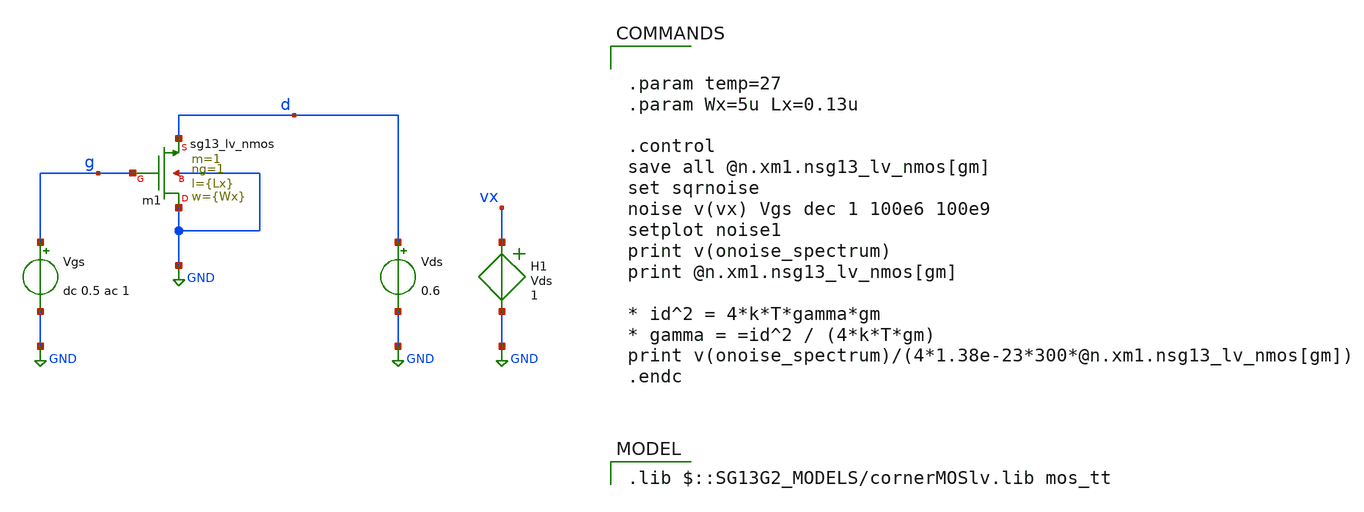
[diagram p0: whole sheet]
** sch_path: 4_Technology/src/tb_sg13_lv_nmos_noise.sch
**.subckt tb_sg13_lv_nmos_noise
Xm1 GND g d GND sg13_lv_nmos w={Wx} l={Lx} ng=1 m=1 mm_ok=1
Vgs g GND dc 0.5 ac 1
Vds d GND 0.6
H1 vx GND Vds 1
**** begin user architecture code
 .lib $::SG13G2_MODELS/cornerMOSlv.lib mos_tt



.param temp=27
.param Wx=5u Lx=0.13u

.control
save all @n.xm1.nsg13_lv_nmos[gm]
set sqrnoise
noise v(vx) Vgs dec 1 100e6 100e9
setplot noise1
print v(onoise_spectrum)
print @n.xm1.nsg13_lv_nmos[gm]

* id^2 = 4*k*T*gamma*gm
* gamma = =id^2 / (4*k*T*gm)
print v(onoise_spectrum)/(4*1.38e-23*300*@n.xm1.nsg13_lv_nmos[gm])
.endc


**** end user architecture code
**.ends
.GLOBAL GND
.end
